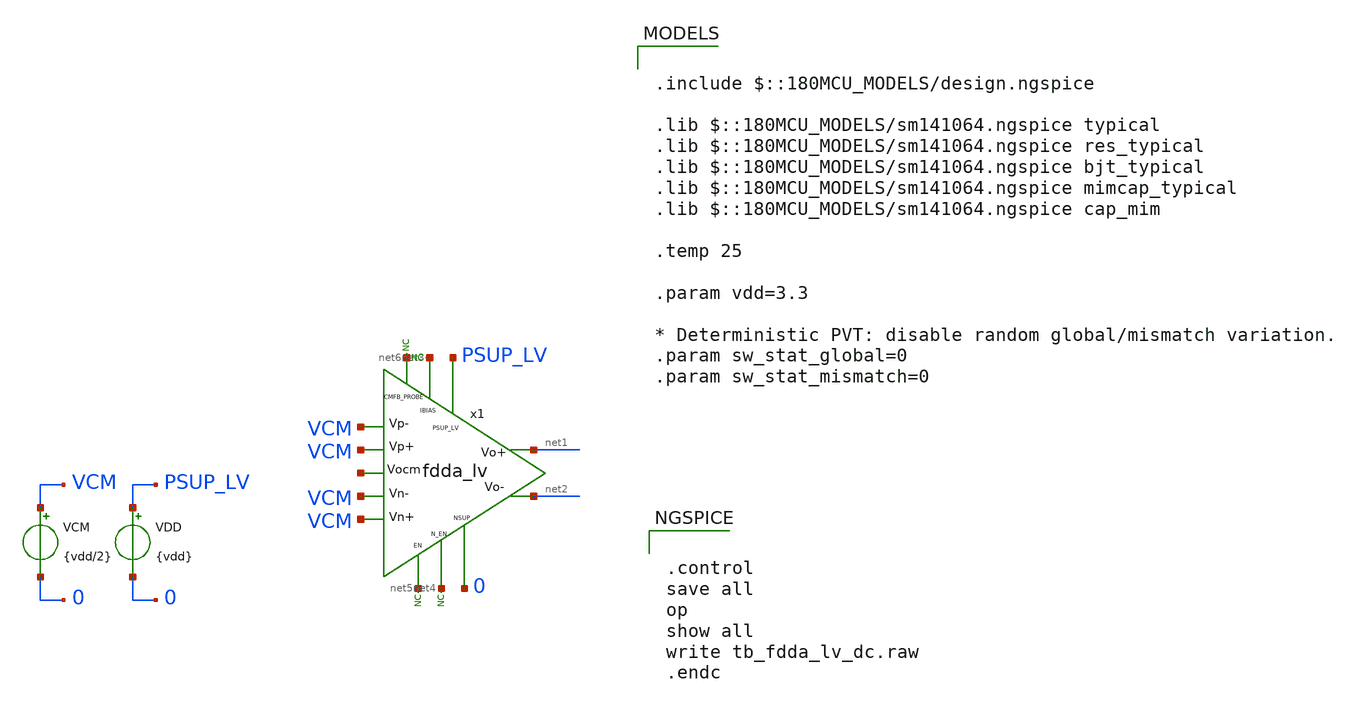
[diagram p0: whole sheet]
** sch_path: xschem/blocks/fdda_lv/tb_fdda_lv_dc.sch
**.subckt tb_fdda_lv_dc
x1 PSUP_LV VCM VCM VCM VCM net1 net2 net3 net4 net5 0 net6 net7 fdda_lv
* noconn #net3
* noconn #net6
* noconn #net5
* noconn #net4
VDD PSUP_LV 0 {vdd}
VCM VCM 0 {vdd/2}
**** begin user architecture code


.control
save all
op
show all
write tb_fdda_lv_dc.raw
.endc



.include $::180MCU_MODELS/design.ngspice

.lib $::180MCU_MODELS/sm141064.ngspice typical
.lib $::180MCU_MODELS/sm141064.ngspice res_typical
.lib $::180MCU_MODELS/sm141064.ngspice bjt_typical
.lib $::180MCU_MODELS/sm141064.ngspice mimcap_typical
.lib $::180MCU_MODELS/sm141064.ngspice cap_mim

.temp 25

.param vdd=3.3

* Deterministic PVT: disable random global/mismatch variation.
.param sw_stat_global=0
.param sw_stat_mismatch=0


**** end user architecture code
**.ends
.end
